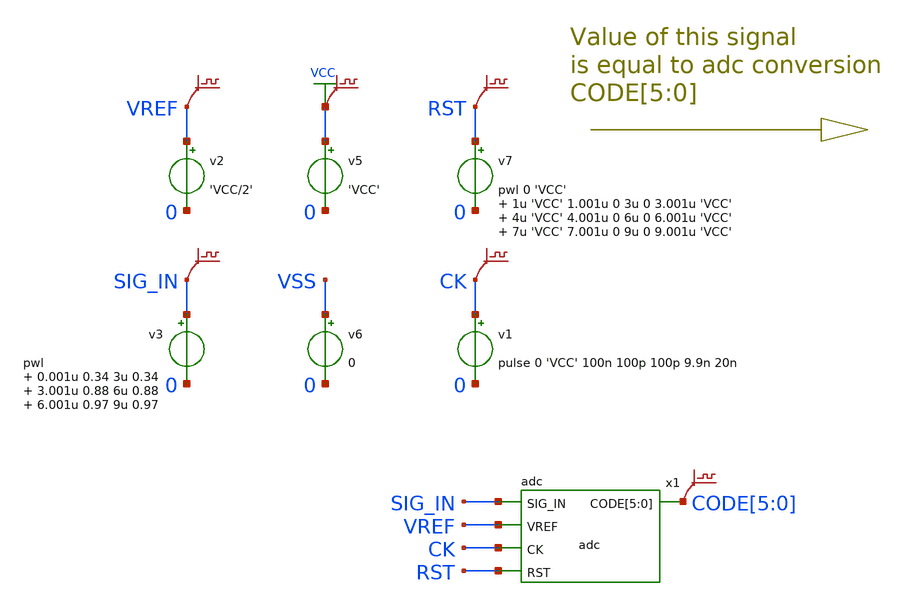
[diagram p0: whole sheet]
** sch_path: xschem-src/xschem_library/ngspice/delta_sigma.sch
* Copyright (C) 1998-2026 Stefan Frederik Schippers
* This program is free software; you can redistribute it and/or modify
* it under the terms of the GNU General Public License as published by
* the Free Software Foundation; either version 2 of the License, or
* (at your option) any later version.
* This program is distributed in the hope that it will be useful,
* but WITHOUT ANY WARRANTY; without even the implied warranty of
* MERCHANTABILITY or FITNESS FOR A PARTICULAR PURPOSE.  See the
* GNU General Public License for more details.
* You should have received a copy of the GNU General Public License
* along with this program; if not, write to the Free Software
**.subckt delta_sigma
v2 VREF 0 'VCC/2'
v3 SIG_IN 0 pwl 0.001u 0.34 3u 0.34 3.001u 0.88 6u 0.88 6.001u 0.97 9u 0.97
v1 CK 0 pulse 0 'VCC' 100n 100p 100p 9.9n 20n
v5 VCC 0 'VCC'
v6 VSS 0 0
v7 RST 0 pwl 0 'VCC' 1u 'VCC' 1.001u 0 3u 0 3.001u 'VCC' 4u 'VCC' 4.001u 0 6u 0 6.001u 'VCC' 7u 'VCC'
+ 7.001u 0 9u 0 9.001u 'VCC'
x1 CODE[5] CODE[4] CODE[3] CODE[2] CODE[1] CODE[0] SIG_IN VREF CK RST adc
.save v(vref)
.save v(vcc)
.save v(sig_in)
.save v(ck)
.save v(rst)
.save v(code[5])
.save v(code[4])
.save v(code[3])
.save v(code[2])
.save v(code[1])
.save v(code[0])
**** begin user architecture code



** download the models from:
** https://ptm.asu.edu/modelcard/65nm_bulk.txt
.include models_65nm.txt
.model switch sw vt='VCC/2' vh=0.2 ron=1000 roff=1G
.param VCC=1.2
.option method=GEAR
.measure tran avg1 AVG v(x1.qn) from=1u to=3u
.measure tran avg2 AVG v(x1.qn) from=4u to=6u
.measure tran avg3 AVG v(x1.qn) from=7u to=9u
.control
  tran 0.2n 9u uic
  write delta_sigma.raw
  set appendwrite
  save all
  op
  write delta_sigma.raw
  quit 0
.endc



**** end user architecture code
**.ends

* expanding   symbol:  adc.sym # of pins=5
** sym_path: xschem-src/xschem_library/ngspice/adc.sym
** sch_path: xschem-src/xschem_library/ngspice/adc.sch
.subckt adc CODE[5] CODE[4] CODE[3] CODE[2] CODE[1] CODE[0] SIG_IN VREF CK RST
*.opin CODE[5],CODE[4],CODE[3],CODE[2],CODE[1],CODE[0]
*.ipin CK
*.ipin RST
*.ipin VREF
*.ipin SIG_IN
x1 COMP CK Q 0 flip_flop_ngspice
x2 CK COUNT[5] COUNT[4] COUNT[3] COUNT[2] COUNT[1] COUNT[0] QN net4 counter_6bit_ngspice
x4[5] COUNT[5] RSTI CODE[5] RST flip_flop_ngspice
x4[4] COUNT[4] RSTI CODE[4] RST flip_flop_ngspice
x4[3] COUNT[3] RSTI CODE[3] RST flip_flop_ngspice
x4[2] COUNT[2] RSTI CODE[2] RST flip_flop_ngspice
x4[1] COUNT[1] RSTI CODE[1] RST flip_flop_ngspice
x4[0] COUNT[0] RSTI CODE[0] RST flip_flop_ngspice
x4 CK C[5] C[4] C[3] C[2] C[1] C[0] VCC RST counter_6bit_ngspice
x5 net2 C[5] C[4] C[3] and3_ngspice ROUT=1000
x6 net1 C[2] C[1] C[0] and3_ngspice ROUT=1000
x7 net5 net2 net1 and_ngspice ROUT=1000
x8 net3 RST net5 or_ngspice ROUT=1000
x9 VCC net3 RSTI RST flip_flop_ngspice
.save v(q)
.save v(comp)
.save v(rsti)
x11 QN Q inv_ngspice RUP=1000 RDOWN=1000
.save v(qn)
c10 INTEG FB 1e-12 m=1
R4 FB SIG_IN 60k m=1
R5 FB Q 60k m=1
.save v(integ)
.save v(fb)
x41 VREF INTEG FB opamp_65nm
x42 INTEG COMP VREF comp_65nm
.save v(count[5])
.save v(count[4])
.save v(count[3])
.save v(count[2])
.save v(count[1])
.save v(count[0])
x3 net4 RST RSTI or_ngspice ROUT=1000
.ends


* expanding   symbol:  flip_flop_ngspice.sym # of pins=4
** sym_path: xschem-src/xschem_library/ngspice/flip_flop_ngspice.sym
** sch_path: xschem-src/xschem_library/ngspice/flip_flop_ngspice.sch
.subckt flip_flop_ngspice D CLK Q RST
*.ipin D
*.ipin CLK
*.ipin RST
*.opin Q
x2 DI keeper_ngspice
S1 net2 net3 VCC CLK SWITCH
S2 QI net1 CLK 0 SWITCH
x3 QI keeper_ngspice
x4 Q QI buf_ngspice RUP=100 RDOWN=100
S3 QI 0 RST 0 SWITCH
x1 net1 DI buf_ngspice RUP=1000 RDOWN=1000
S4 DI net2 VCC RST SWITCH
S5 DI 0 RST 0 SWITCH
x5 net3 D buf_ngspice RUP=1000 RDOWN=1000
.ends


* expanding   symbol:  counter_6bit_ngspice.sym # of pins=4
** sym_path: xschem-src/xschem_library/ngspice/counter_6bit_ngspice.sym
** sch_path: xschem-src/xschem_library/ngspice/counter_6bit_ngspice.sch
.subckt counter_6bit_ngspice CK COUNT[5] COUNT[4] COUNT[3] COUNT[2] COUNT[1] COUNT[0] D RST
*.ipin RST
*.ipin D
*.opin COUNT[5],COUNT[4],COUNT[3],COUNT[2],COUNT[1],COUNT[0]
*.ipin CK
x2[5] S[5] CK COUNT[5] RST flip_flop_ngspice
x2[4] S[4] CK COUNT[4] RST flip_flop_ngspice
x2[3] S[3] CK COUNT[3] RST flip_flop_ngspice
x2[2] S[2] CK COUNT[2] RST flip_flop_ngspice
x2[1] S[1] CK COUNT[1] RST flip_flop_ngspice
x2[0] S[0] CK COUNT[0] RST flip_flop_ngspice
x1[5] COUNT[5] S[5] COUT[5] COUT[4] half_adder_ngspice
x1[4] COUNT[4] S[4] COUT[4] COUT[3] half_adder_ngspice
x1[3] COUNT[3] S[3] COUT[3] COUT[2] half_adder_ngspice
x1[2] COUNT[2] S[2] COUT[2] COUT[1] half_adder_ngspice
x1[1] COUNT[1] S[1] COUT[1] COUT[0] half_adder_ngspice
x1[0] COUNT[0] S[0] COUT[0] D half_adder_ngspice
.ends


* expanding   symbol:  and3_ngspice.sym # of pins=4
** sym_path: xschem-src/xschem_library/ngspice/and3_ngspice.sym
** sch_path: xschem-src/xschem_library/ngspice/and3_ngspice.sch
.subckt and3_ngspice Y A B C  ROUT=1000
*.ipin A
*.opin Y
*.ipin B
*.ipin C
B1 net1 0 V = 'VCC/2*(1+tanh((min(V(C1),min(V(A1),V(B1)))-VCC/2)*100))'
R1 Y1 net1 'ROUT' m=1
C1 A1 0 8f m=1
C2 B1 0 8f m=1
C3 Y1 0 8f m=1
C4 C1 0 8f m=1
V1 A1 A 0
V2 B1 B 0
V3 C1 C 0
V4 Y Y1 0
.ends


* expanding   symbol:  and_ngspice.sym # of pins=3
** sym_path: xschem-src/xschem_library/ngspice/and_ngspice.sym
** sch_path: xschem-src/xschem_library/ngspice/and_ngspice.sch
.subckt and_ngspice Y A B  ROUT=1000
*.ipin A
*.opin Y
*.ipin B
B1 net1 0 V = 'VCC/2*(1+tanh((min(V(A1),V(B1))-VCC/2)*100))'
R1 Y1 net1 'ROUT' m=1
C1 A1 0 8f m=1
C2 B1 0 8f m=1
C3 Y1 0 8f m=1
V1 A1 A 0
V2 B1 B 0
V3 Y Y1 0
.ends


* expanding   symbol:  or_ngspice.sym # of pins=3
** sym_path: xschem-src/xschem_library/ngspice/or_ngspice.sym
** sch_path: xschem-src/xschem_library/ngspice/or_ngspice.sch
.subckt or_ngspice Y A B  ROUT=1000
*.ipin A
*.opin Y
*.ipin B
B1 net1 0 V = 'VCC/2*(1+tanh((max(V(A1),V(B1))-VCC/2)*100))'
R1 Y1 net1 'ROUT' m=1
C1 A1 0 8f m=1
C2 B1 0 8f m=1
C3 Y1 0 8f m=1
V1 A1 A 0
V2 B1 B 0
V3 Y Y1 0
.ends


* expanding   symbol:  inv_ngspice.sym # of pins=2
** sym_path: xschem-src/xschem_library/ngspice/inv_ngspice.sym
** sch_path: xschem-src/xschem_library/ngspice/inv_ngspice.sch
.subckt inv_ngspice Y A  RUP=2000 RDOWN=1000
*.ipin A
*.opin Y
B1 X1 0 V = 'VCC/2*(1-tanh((V(A1)-VCC/2)*100))'
C1 A1 0 8f m=1
C2 Y1 0 8f m=1
V1 Y Y1 0
.save i(v1)
V2 A1 A 0
.save i(v2)
B2 X1 Y1 I = 'v(X1,Y1) > 0 ? v(X1,Y1) / RUP : v(X1,Y1) / RDOWN'
.ends


* expanding   symbol:  opamp_65nm.sym # of pins=3
** sym_path: xschem-src/xschem_library/ngspice/opamp_65nm.sym
** sch_path: xschem-src/xschem_library/ngspice/opamp_65nm.sch
.subckt opamp_65nm PLUS OUT MINUS
*.ipin PLUS
*.ipin MINUS
*.opin OUT
M1 S GN1 0 0 nmos w=4u l=0.4u m=1
M2 GN1 GN1 0 0 nmos w=4u l=0.4u m=1
I0 VCC GN1 30u
M3 net1 MINUS S 0 nmos w=1.5u l=0.2u m=1
M4 G PLUS S 0 nmos w=1.5u l=0.2u m=1
M5 net1 net1 VCC VCC pmos w=6u l=0.3u m=1
M6 G net1 VCC VCC pmos w=6u l=0.3u m=1
M8 OUT G VCC VCC pmos w=6u l=0.4u m=1
.save v(gn1)
.save v(net1)
M7 OUT GN1 0 0 nmos w=4u l=0.4u m=1
R1 OUT net2 5k m=1
C1 G net2 150f m=1
C2 GN1 0 200f m=1
.save v(s)
.ends


* expanding   symbol:  comp_65nm.sym # of pins=3
** sym_path: comp_65nm.sym
** sch_path: comp_65nm.sch
.subckt comp_65nm PLUS OUT MINUS
*.ipin PLUS
*.ipin MINUS
*.opin OUT
M1 net1 GN1 0 0 nmos w=4u l=0.4u m=1
M2 GN1 GN1 0 0 nmos w=4u l=0.4u m=1
I0 VCC GN1 30u
M3 net2 MINUS net1 0 nmos w=1.5u l=0.2u m=1
M4 net3 PLUS net1 0 nmos w=1.5u l=0.2u m=1
M5 net2 net2 VCC VCC pmos w=6u l=0.3u m=1
M6 net3 net2 VCC VCC pmos w=6u l=0.3u m=1
M14 net4 net3 VCC VCC pmos w=6u l=0.3u m=1
.save v(gn1)
.save v(net2)
M7 net4 GN1 0 0 nmos w=4u l=0.4u m=1
M8 net5 net4 0 0 nmos w=1u l=0.4u m=1
M9 net5 net4 VCC VCC pmos w=2u l=0.4u m=1
M10 OUT net5 0 0 nmos w=1u l=0.4u m=1
M11 OUT net5 VCC VCC pmos w=2u l=0.4u m=1
M13 net4 net4 net5 0 nmos w=2u l=0.1u m=1
.save v(net5)
.save v(net4)
M12 net5 net5 net4 0 nmos w=2u l=0.1u m=1
.save v(net1)
C2 GN1 0 200f m=1
.ends


* expanding   symbol:  keeper_ngspice.sym # of pins=1
** sym_path: xschem-src/xschem_library/ngspice/keeper_ngspice.sym
** sch_path: xschem-src/xschem_library/ngspice/keeper_ngspice.sch
.subckt keeper_ngspice A
*.ipin A
x1 Y A inv_ngspice RUP=2000 RDOWN=1000
x2 A Y inv_ngspice RUP=300k RDOWN=200k
.ends


* expanding   symbol:  buf_ngspice.sym # of pins=2
** sym_path: xschem-src/xschem_library/ngspice/buf_ngspice.sym
** sch_path: xschem-src/xschem_library/ngspice/buf_ngspice.sch
.subckt buf_ngspice Y A  RUP=2000 RDOWN=1000
*.ipin A
*.opin Y
B1 X1 0 V = 'VCC/2*(1+tanh((V(A1)-VCC/2)*100))'
C3 Y1 0 8f m=1
C1 A1 0 4f m=1
V1 Y Y1 0
V2 A1 A 0
B2 X1 Y1 I = 'v(X1,Y1) > 0 ? v(X1,Y1) / RUP : v(X1,Y1) / RDOWN'
.ends


* expanding   symbol:  half_adder_ngspice.sym # of pins=4
** sym_path: xschem-src/xschem_library/ngspice/half_adder_ngspice.sym
** sch_path: xschem-src/xschem_library/ngspice/half_adder_ngspice.sch
.subckt half_adder_ngspice A S COUT B
*.ipin A
*.ipin B
*.opin S
*.opin COUT
x1 S A B xor_ngspice ROUT=1000
x2 COUT A B and_ngspice ROUT=1000
.ends


* expanding   symbol:  xor_ngspice.sym # of pins=3
** sym_path: xschem-src/xschem_library/ngspice/xor_ngspice.sym
** sch_path: xschem-src/xschem_library/ngspice/xor_ngspice.sch
.subckt xor_ngspice Y A B  ROUT=1000
*.ipin A
*.opin Y
*.ipin B
B1 net1 0 V = 'VCC/2*(1+tanh((abs(V(A1)-V(B1))-VCC/2)*100))'
R1 Y1 net1 'ROUT' m=1
C1 A1 0 8f m=1
C2 B1 0 8f m=1
C3 Y1 0 8f m=1
V1 A1 A 0
V2 B1 B 0
V3 Y Y1 0
.ends

.GLOBAL VCC
.end
